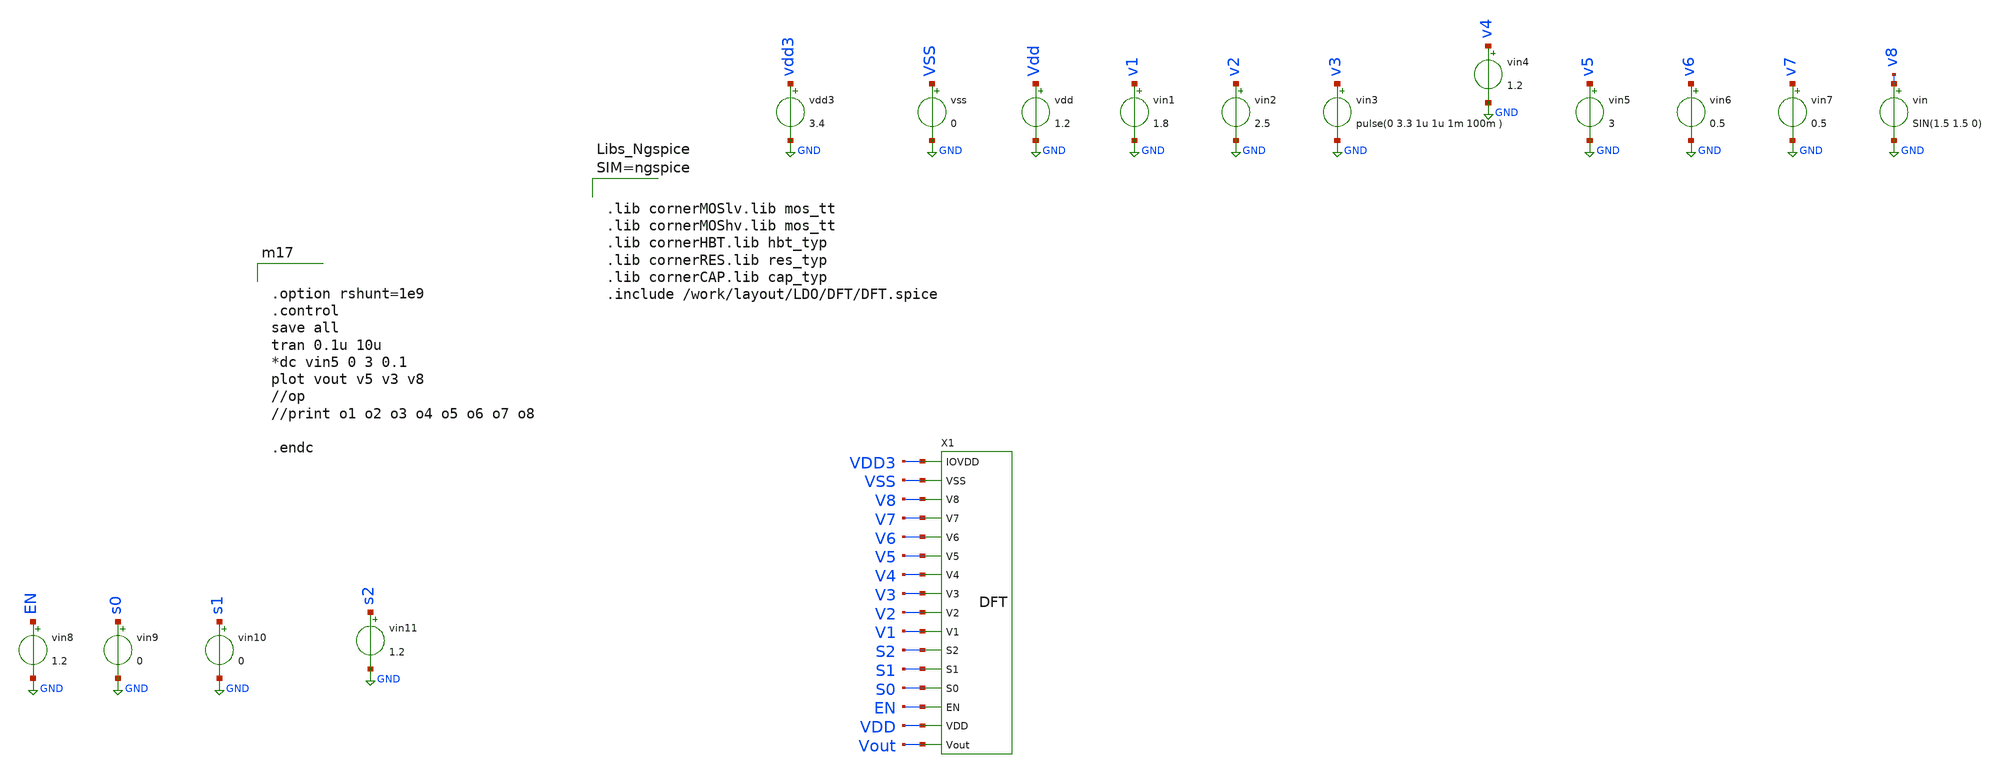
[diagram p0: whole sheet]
** sch_path: dependencies/DFT/DFT-main/testbenches/DFT_gds_tb.sch
**.subckt DFT_gds_tb
vin v8 GND SIN(1.5 1.5 0)
vin1 v1 GND 1.8
vin2 v2 GND 2.5
vin3 v3 GND pulse(0 3.3 1u 1u 1m 100m )
vin4 v4 GND 1.2
vin5 v5 GND 3
vin6 v6 GND 0.5
vin7 v7 GND 0.5
vin8 EN GND 1.2
vin9 s0 GND 0
vin10 s1 GND 0
vin11 s2 GND 1.2
vdd Vdd GND 1.2
vss VSS GND 0
vdd3 vdd3 GND 3.4
X1 VDD3 VSS V8 V7 V6 V5 V4 V3 V2 V1 S2 S1 S0 EN VDD Vout DFT
**** begin user architecture code



.lib cornerMOSlv.lib mos_tt
.lib cornerMOShv.lib mos_tt
.lib cornerHBT.lib hbt_typ
.lib cornerRES.lib res_typ
.lib cornerCAP.lib cap_typ
.include /work/layout/LDO/DFT/DFT.spice





.option rshunt=1e9
.control
save all
tran 0.1u 10u
*dc vin5 0 3 0.1
plot vout v5 v3 v8
//op
//print o1 o2 o3 o4 o5 o6 o7 o8

.endc

**** end user architecture code
**.ends
.GLOBAL GND
.end
